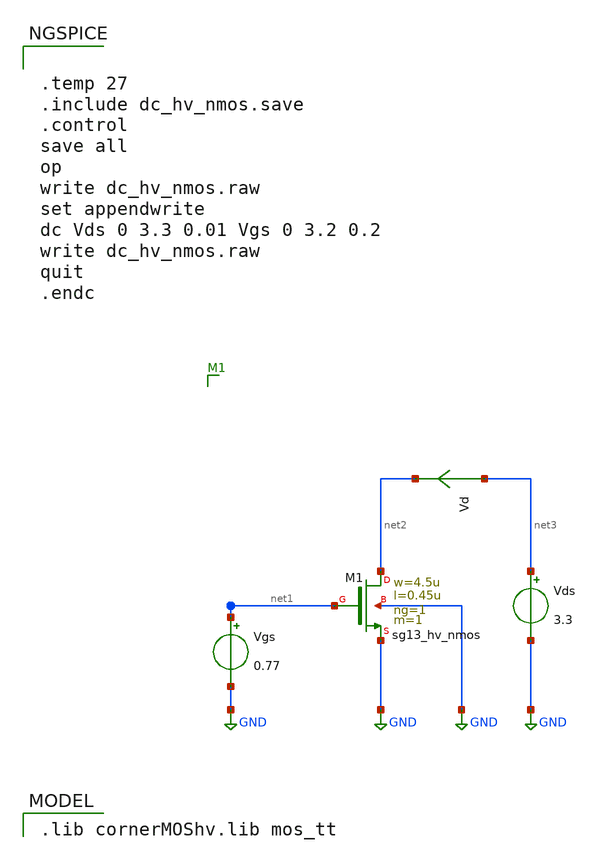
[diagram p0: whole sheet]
** sch_path: xschem/dc_hv_nmos.sch
* (c) 2023-2025 Harald Pretl, Apache-2.0 license
**.subckt dc_hv_nmos
Vgs net1 GND 0.77
Vds net3 GND 3.3
Vd net3 net2 0
.save i(vd)
XM1 net2 net1 GND GND sg13_hv_nmos w=4.5u l=0.45u ng=1 m=1 mm_ok=1
**** begin user architecture code
 .lib cornerMOShv.lib mos_tt



.temp 27
.include dc_hv_nmos.save
.control
save all
op
write dc_hv_nmos.raw
set appendwrite
dc Vds 0 3.3 0.01 Vgs 0 3.2 0.2
write dc_hv_nmos.raw
quit
.endc


**** end user architecture code
**.ends
.GLOBAL GND
.end
